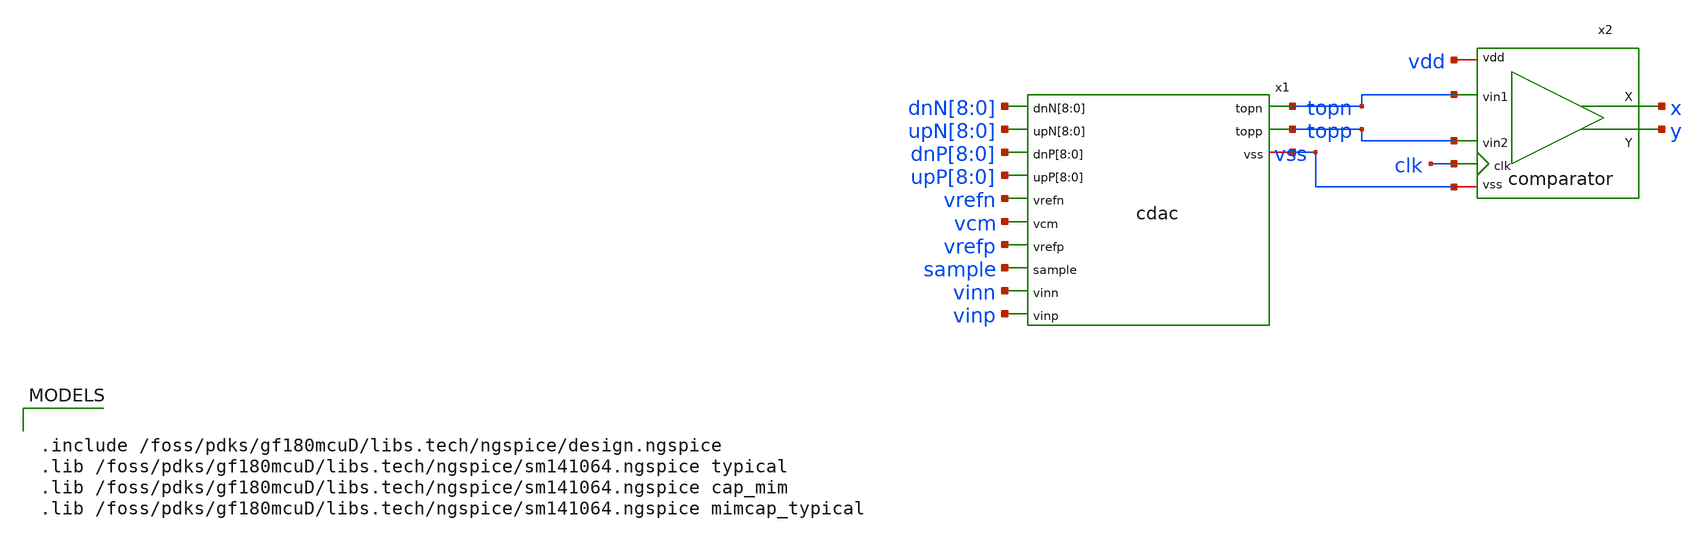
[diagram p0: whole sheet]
** sch_path: designs/libs/core_analog/saradc/tb/cdac_comp_tb.sch
**.subckt cdac_comp_tb
x1 dnN[8] dnN[7] dnN[6] dnN[5] dnN[4] dnN[3] dnN[2] dnN[1] dnN[0] upN[8] upN[7] upN[6] upN[5] upN[4]
+ upN[3] upN[2] upN[1] upN[0] dnP[8] dnP[7] dnP[6] dnP[5] dnP[4] dnP[3] dnP[2] dnP[1] dnP[0] upP[8] upP[7]
+ upP[6] upP[5] upP[4] upP[3] upP[2] upP[1] upP[0] topn topp vss vrefn vcm vrefp sample vinn vinp cdac
x2 vdd vss x topn y topp clk comparator
**** begin user architecture code


.include /foss/pdks/gf180mcuD/libs.tech/ngspice/design.ngspice
.lib /foss/pdks/gf180mcuD/libs.tech/ngspice/sm141064.ngspice typical
.lib /foss/pdks/gf180mcuD/libs.tech/ngspice/sm141064.ngspice cap_mim
.lib /foss/pdks/gf180mcuD/libs.tech/ngspice/sm141064.ngspice mimcap_typical




* ============ CDAC + Comparator open-loop SAR TB ============
* Two forced-code tests share the bias/clock/control below.
* To switch test: comment one TEST block, uncomment the other.
* sample 0..9n ; comparator evals at 15,25,..,105n ; cap switched at 20,30,..,100n
* SAR rule:  bit=1 -> dnP[i]+upN[i] (lower vdiff) ;  bit=0 -> upP[i]+dnN[i] (raise) ;  cap 8->0

* ---- shared supplies / references / clock / loads ----
Vvdd   VDD   0 3.3
Vvss   vss   0 0
Vvrefp vrefp 0 1
Vvrefn vrefn 0 0
Vvcm   vcm   0 0.5
Vsample sample 0 PWL(0 3.3 9n 3.3 9.05n 0)
Vclk CLK 0 pulse(0 3.3 15n 50p 50p 4n 10n)
Cx X 0 20f
Cy Y 0 20f
.param CM = 1.65

* ============ TEST A : code 682 = 1010101010   (DISABLED) ============
* .param vid = 0.333
* Vvinp  vinp  0 'CM+vid/2'
* Vvinn  vinn  0 'CM-vid/2'
* VdnP8 dnP[8] 0 PWL(0 0 19.99n 0 20n 3.3)
* VupN8 upN[8] 0 PWL(0 0 19.99n 0 20n 3.3)
* VupP7 upP[7] 0 PWL(0 0 29.99n 0 30n 3.3)
* VdnN7 dnN[7] 0 PWL(0 0 29.99n 0 30n 3.3)
* VdnP6 dnP[6] 0 PWL(0 0 39.99n 0 40n 3.3)
* VupN6 upN[6] 0 PWL(0 0 39.99n 0 40n 3.3)
* VupP5 upP[5] 0 PWL(0 0 49.99n 0 50n 3.3)
* VdnN5 dnN[5] 0 PWL(0 0 49.99n 0 50n 3.3)
* VdnP4 dnP[4] 0 PWL(0 0 59.99n 0 60n 3.3)
* VupN4 upN[4] 0 PWL(0 0 59.99n 0 60n 3.3)
* VupP3 upP[3] 0 PWL(0 0 69.99n 0 70n 3.3)
* VdnN3 dnN[3] 0 PWL(0 0 69.99n 0 70n 3.3)
* VdnP2 dnP[2] 0 PWL(0 0 79.99n 0 80n 3.3)
* VupN2 upN[2] 0 PWL(0 0 79.99n 0 80n 3.3)
* VupP1 upP[1] 0 PWL(0 0 89.99n 0 90n 3.3)
* VdnN1 dnN[1] 0 PWL(0 0 89.99n 0 90n 3.3)
* VdnP0 dnP[0] 0 PWL(0 0 99.99n 0 100n 3.3)
* VupN0 upN[0] 0 PWL(0 0 99.99n 0 100n 3.3)
* VupP8 upP[8] 0 0
* VupP6 upP[6] 0 0
* VupP4 upP[4] 0 0
* VupP2 upP[2] 0 0
* VupP0 upP[0] 0 0
* VdnP7 dnP[7] 0 0
* VdnP5 dnP[5] 0 0
* VdnP3 dnP[3] 0 0
* VdnP1 dnP[1] 0 0
* VupN7 upN[7] 0 0
* VupN5 upN[5] 0 0
* VupN3 upN[3] 0 0
* VupN1 upN[1] 0 0
* VdnN8 dnN[8] 0 0
* VdnN6 dnN[6] 0 0
* VdnN4 dnN[4] 0 0
* VdnN2 dnN[2] 0 0
* VdnN0 dnN[0] 0 0

* ============ TEST B : code 992 = 1111100000   (ACTIVE) ============
* vid = bin-center = (992-512)*LSB + LSB/2 = 0.9375 + 0.0009766
.param vid = 0.9385
Vvinp  vinp  0 'CM+vid/2'
Vvinn  vinn  0 'CM-vid/2'
VdnP8 dnP[8] 0 PWL(0 0 19.99n 0 20n 3.3)
VupN8 upN[8] 0 PWL(0 0 19.99n 0 20n 3.3)
VdnP7 dnP[7] 0 PWL(0 0 29.99n 0 30n 3.3)
VupN7 upN[7] 0 PWL(0 0 29.99n 0 30n 3.3)
VdnP6 dnP[6] 0 PWL(0 0 39.99n 0 40n 3.3)
VupN6 upN[6] 0 PWL(0 0 39.99n 0 40n 3.3)
VdnP5 dnP[5] 0 PWL(0 0 49.99n 0 50n 3.3)
VupN5 upN[5] 0 PWL(0 0 49.99n 0 50n 3.3)
VdnP4 dnP[4] 0 PWL(0 0 59.99n 0 60n 3.3)
VupN4 upN[4] 0 PWL(0 0 59.99n 0 60n 3.3)
VupP3 upP[3] 0 PWL(0 0 69.99n 0 70n 3.3)
VdnN3 dnN[3] 0 PWL(0 0 69.99n 0 70n 3.3)
VupP2 upP[2] 0 PWL(0 0 79.99n 0 80n 3.3)
VdnN2 dnN[2] 0 PWL(0 0 79.99n 0 80n 3.3)
VupP1 upP[1] 0 PWL(0 0 89.99n 0 90n 3.3)
VdnN1 dnN[1] 0 PWL(0 0 89.99n 0 90n 3.3)
VupP0 upP[0] 0 PWL(0 0 99.99n 0 100n 3.3)
VdnN0 dnN[0] 0 PWL(0 0 99.99n 0 100n 3.3)
VupP8 upP[8] 0 0
VupP7 upP[7] 0 0
VupP6 upP[6] 0 0
VupP5 upP[5] 0 0
VupP4 upP[4] 0 0
VdnP3 dnP[3] 0 0
VdnP2 dnP[2] 0 0
VdnP1 dnP[1] 0 0
VdnP0 dnP[0] 0 0
VdnN8 dnN[8] 0 0
VdnN7 dnN[7] 0 0
VdnN6 dnN[6] 0 0
VdnN5 dnN[5] 0 0
VdnN4 dnN[4] 0 0
VupN3 upN[3] 0 0
VupN2 upN[2] 0 0
VupN1 upN[1] 0 0
VupN0 upN[0] 0 0

.control
save all
tran 20p 115n
write cdac_comp_tb.raw
let vdiff  = v(topp)-v(topn)
let vcmtop = (v(topp)+v(topn))/2
* sample each decision ~3.5n into its eval window ; X high => bit 1
meas tran b9 find v(X) at=18.5n
meas tran b8 find v(X) at=28.5n
meas tran b7 find v(X) at=38.5n
meas tran b6 find v(X) at=48.5n
meas tran b5 find v(X) at=58.5n
meas tran b4 find v(X) at=68.5n
meas tran b3 find v(X) at=78.5n
meas tran b2 find v(X) at=88.5n
meas tran b1 find v(X) at=98.5n
meas tran b0 find v(X) at=108.5n
print b9 b8 b7 b6 b5 b4 b3 b2 b1 b0
plot v(CLK) v(X) v(Y)
.endc


**** end user architecture code
**.ends
.end
